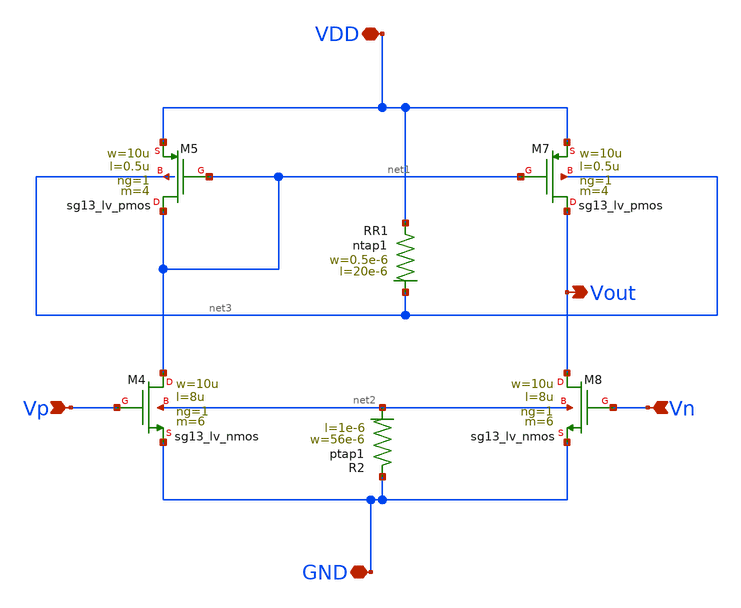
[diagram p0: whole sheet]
** sch_path: Layouts/ib_ctat_ptat/opamp.sch
**.subckt opamp VDD Vp Vn GND Vout
*.iopin VDD
*.ipin Vp
*.ipin Vn
*.iopin GND
*.opin Vout
XM4 net1 Vp GND net2 sg13_lv_nmos w=10u l=8u ng=1 m=6 mm_ok=1
XM5 net1 net1 VDD net3 sg13_lv_pmos w=10u l=0.5u ng=1 m=4 mm_ok=1
XM7 Vout net1 VDD net3 sg13_lv_pmos w=10u l=0.5u ng=1 m=4 mm_ok=1
XM8 Vout Vn GND net2 sg13_lv_nmos w=10u l=8u ng=1 m=6 mm_ok=1
XR1 VDD net3 ntap1 R=19.22 w=0.5e-6 l=20e-6
XR2 GND net2 ptap1 R=5.765 w=56e-6 l=1e-6
**.ends
.end
